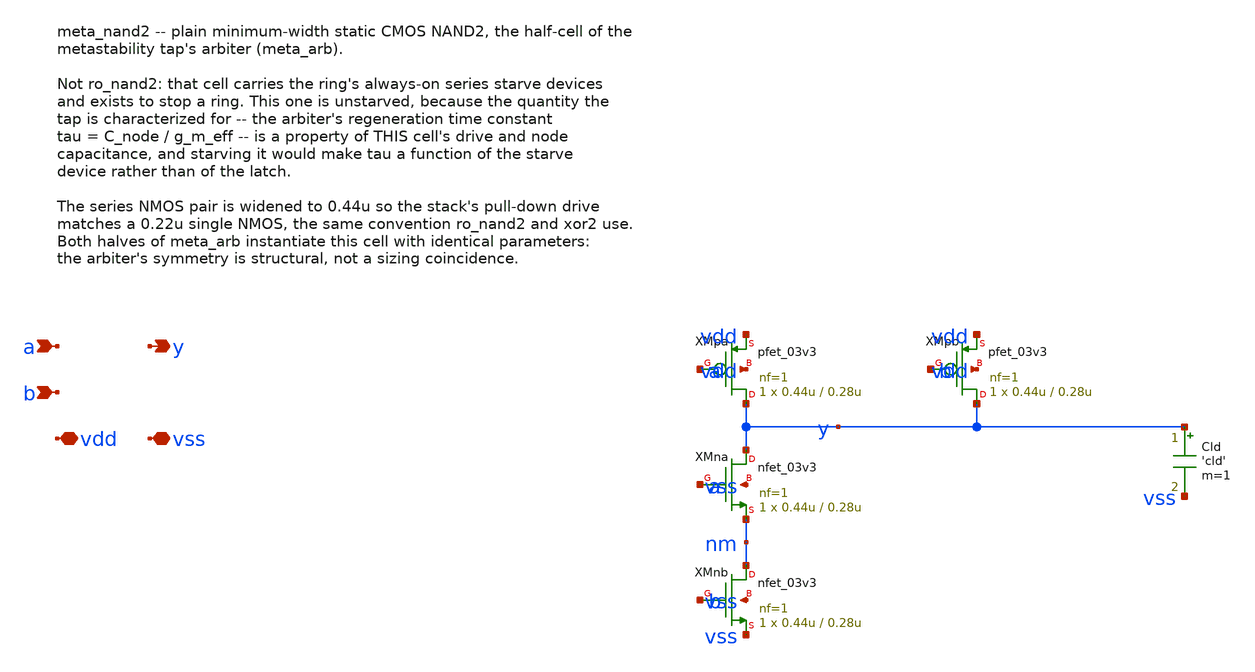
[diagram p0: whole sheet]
** sch_path: design/xschem/meta_nand2.sch
**.subckt meta_nand2 a b y vdd vss
*.ipin a
*.ipin b
*.opin y
*.iopin vdd
*.iopin vss
XMpa y a vdd vdd pfet_03v3 L=0.28u W=0.44u nf=1 ad='int((nf+1)/2) * W/nf * 0.18u' as='int((nf+2)/2) * W/nf * 0.18u'
+ pd='2*int((nf+1)/2) * (W/nf + 0.18u)' ps='2*int((nf+2)/2) * (W/nf + 0.18u)' nrd='0.18u / W' nrs='0.18u / W'
+ sa=0 sb=0 sd=0 m=1
XMpb y b vdd vdd pfet_03v3 L=0.28u W=0.44u nf=1 ad='int((nf+1)/2) * W/nf * 0.18u' as='int((nf+2)/2) * W/nf * 0.18u'
+ pd='2*int((nf+1)/2) * (W/nf + 0.18u)' ps='2*int((nf+2)/2) * (W/nf + 0.18u)' nrd='0.18u / W' nrs='0.18u / W'
+ sa=0 sb=0 sd=0 m=1
XMna y a nm vss nfet_03v3 L=0.28u W=0.44u nf=1 ad='int((nf+1)/2) * W/nf * 0.18u' as='int((nf+2)/2) * W/nf * 0.18u'
+ pd='2*int((nf+1)/2) * (W/nf + 0.18u)' ps='2*int((nf+2)/2) * (W/nf + 0.18u)' nrd='0.18u / W' nrs='0.18u / W'
+ sa=0 sb=0 sd=0 m=1
XMnb nm b vss vss nfet_03v3 L=0.28u W=0.44u nf=1 ad='int((nf+1)/2) * W/nf * 0.18u' as='int((nf+2)/2) * W/nf * 0.18u'
+ pd='2*int((nf+1)/2) * (W/nf + 0.18u)' ps='2*int((nf+2)/2) * (W/nf + 0.18u)' nrd='0.18u / W' nrs='0.18u / W'
+ sa=0 sb=0 sd=0 m=1
Cld y vss 'cld' m=1
**.ends
.end
